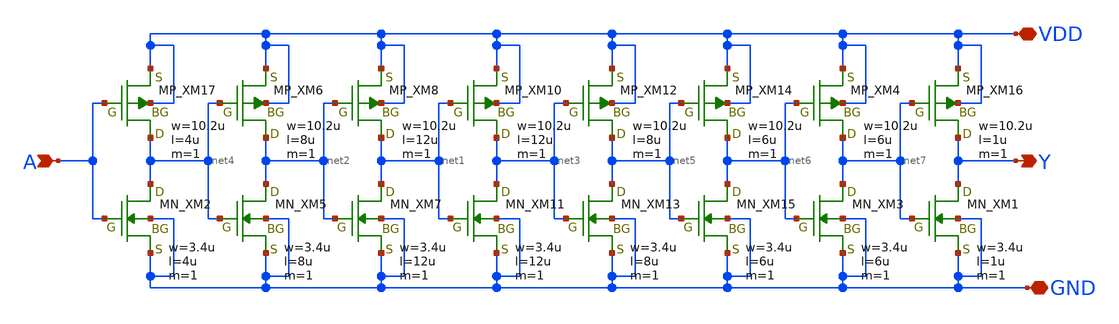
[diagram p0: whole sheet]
** sch_path: openIP62_rev1.0/IP62/Technology/tech/symbols/Xschem/IP62_5_stdcell/DEL4.sch
**.subckt DEL4 A Y VDD GND
*.ipin A
*.opin Y
*.iopin VDD
*.iopin GND
XM17 net4 A VDD VDD PMOS w=10.2u l=4u as=0 ad=0 ps=0 pd=0 nrd=0 nrs=0 m=1
XM6 net2 net4 VDD VDD PMOS w=10.2u l=8u as=0 ad=0 ps=0 pd=0 nrd=0 nrs=0 m=1
XM8 net1 net2 VDD VDD PMOS w=10.2u l=12u as=0 ad=0 ps=0 pd=0 nrd=0 nrs=0 m=1
XM10 net3 net1 VDD VDD PMOS w=10.2u l=12u as=0 ad=0 ps=0 pd=0 nrd=0 nrs=0 m=1
XM12 net5 net3 VDD VDD PMOS w=10.2u l=8u as=0 ad=0 ps=0 pd=0 nrd=0 nrs=0 m=1
XM14 net6 net5 VDD VDD PMOS w=10.2u l=6u as=0 ad=0 ps=0 pd=0 nrd=0 nrs=0 m=1
XM4 net7 net6 VDD VDD PMOS w=10.2u l=6u as=0 ad=0 ps=0 pd=0 nrd=0 nrs=0 m=1
XM16 Y net7 VDD VDD PMOS w=10.2u l=1u as=0 ad=0 ps=0 pd=0 nrd=0 nrs=0 m=1
XM2 net4 A GND GND NMOS w=3.4u l=4u as=0 ad=0 ps=0 pd=0 nrd=0 nrs=0 m=1
XM5 net2 net4 GND GND NMOS w=3.4u l=8u as=0 ad=0 ps=0 pd=0 nrd=0 nrs=0 m=1
XM7 net1 net2 GND GND NMOS w=3.4u l=12u as=0 ad=0 ps=0 pd=0 nrd=0 nrs=0 m=1
XM11 net3 net1 GND GND NMOS w=3.4u l=12u as=0 ad=0 ps=0 pd=0 nrd=0 nrs=0 m=1
XM13 net5 net3 GND GND NMOS w=3.4u l=8u as=0 ad=0 ps=0 pd=0 nrd=0 nrs=0 m=1
XM15 net6 net5 GND GND NMOS w=3.4u l=6u as=0 ad=0 ps=0 pd=0 nrd=0 nrs=0 m=1
XM3 net7 net6 GND GND NMOS w=3.4u l=6u as=0 ad=0 ps=0 pd=0 nrd=0 nrs=0 m=1
XM1 Y net7 GND GND NMOS w=3.4u l=1u as=0 ad=0 ps=0 pd=0 nrd=0 nrs=0 m=1
**.ends
.end
